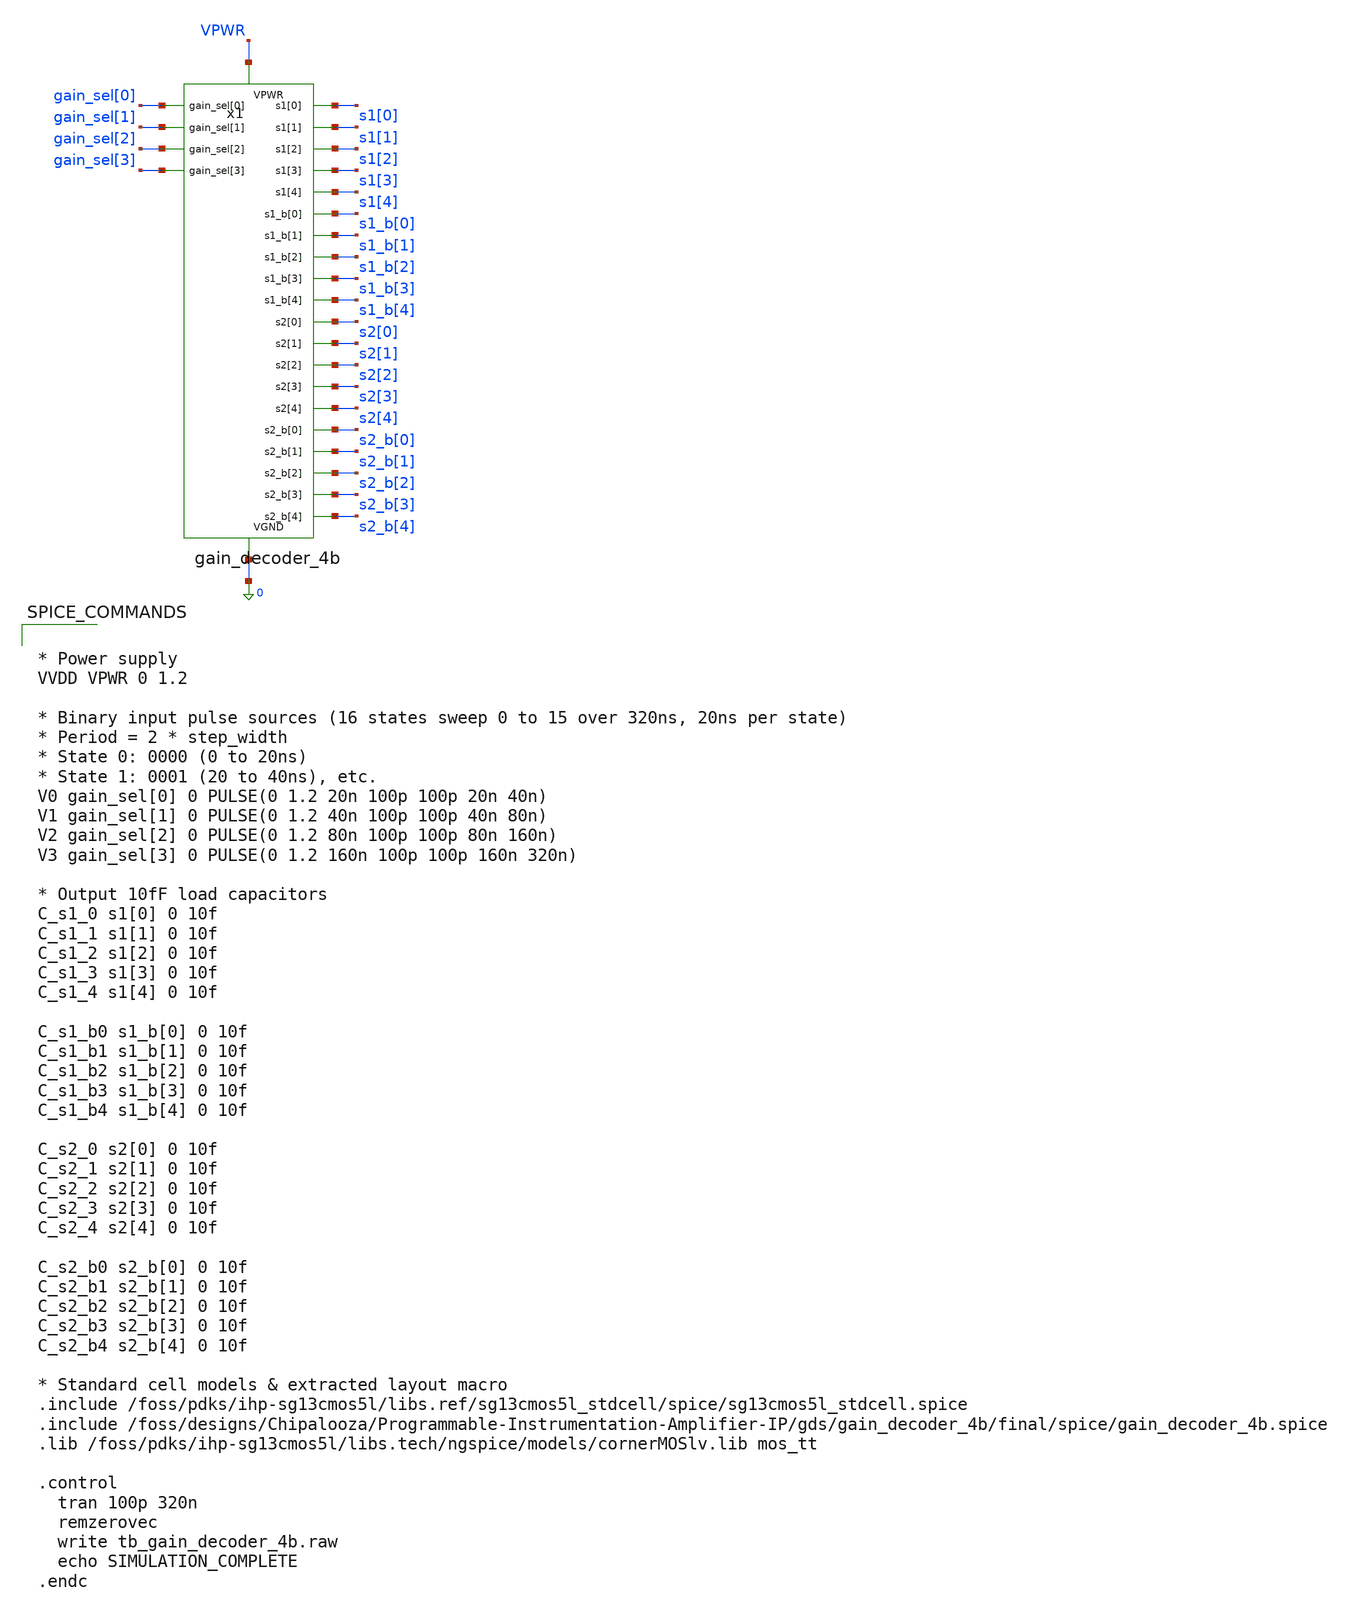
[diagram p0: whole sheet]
** sch_path: xschem/gain_decoder_4b/tb_gain_decoder_4b.sch
**.subckt tb_gain_decoder_4b
x1 0 VPWR gain_sel[0] gain_sel[1] gain_sel[2] gain_sel[3] s1[0] s1[1] s1[2] s1[3] s1[4] s1_b[0]
+ s1_b[1] s1_b[2] s1_b[3] s1_b[4] s2[0] s2[1] s2[2] s2[3] s2[4] s2_b[0] s2_b[1] s2_b[2] s2_b[3] s2_b[4]
+ gain_decoder_4b
**** begin user architecture code


* Power supply
VVDD VPWR 0 1.2

* Binary input pulse sources (16 states sweep 0 to 15 over 320ns, 20ns per state)
* Period = 2 * step_width
* State 0: 0000 (0 to 20ns)
* State 1: 0001 (20 to 40ns), etc.
V0 gain_sel[0] 0 PULSE(0 1.2 20n 100p 100p 20n 40n)
V1 gain_sel[1] 0 PULSE(0 1.2 40n 100p 100p 40n 80n)
V2 gain_sel[2] 0 PULSE(0 1.2 80n 100p 100p 80n 160n)
V3 gain_sel[3] 0 PULSE(0 1.2 160n 100p 100p 160n 320n)

* Output 10fF load capacitors
C_s1_0 s1[0] 0 10f
C_s1_1 s1[1] 0 10f
C_s1_2 s1[2] 0 10f
C_s1_3 s1[3] 0 10f
C_s1_4 s1[4] 0 10f

C_s1_b0 s1_b[0] 0 10f
C_s1_b1 s1_b[1] 0 10f
C_s1_b2 s1_b[2] 0 10f
C_s1_b3 s1_b[3] 0 10f
C_s1_b4 s1_b[4] 0 10f

C_s2_0 s2[0] 0 10f
C_s2_1 s2[1] 0 10f
C_s2_2 s2[2] 0 10f
C_s2_3 s2[3] 0 10f
C_s2_4 s2[4] 0 10f

C_s2_b0 s2_b[0] 0 10f
C_s2_b1 s2_b[1] 0 10f
C_s2_b2 s2_b[2] 0 10f
C_s2_b3 s2_b[3] 0 10f
C_s2_b4 s2_b[4] 0 10f

* Standard cell models & extracted layout macro
.include /foss/pdks/ihp-sg13cmos5l/libs.ref/sg13cmos5l_stdcell/spice/sg13cmos5l_stdcell.spice
.include /foss/designs/Chipalooza/Programmable-Instrumentation-Amplifier-IP/gds/gain_decoder_4b/final/spice/gain_decoder_4b.spice
.lib /foss/pdks/ihp-sg13cmos5l/libs.tech/ngspice/models/cornerMOSlv.lib mos_tt

.control
  tran 100p 320n
  remzerovec
  write tb_gain_decoder_4b.raw
  echo SIMULATION_COMPLETE
.endc


**** end user architecture code
**.ends
.end
